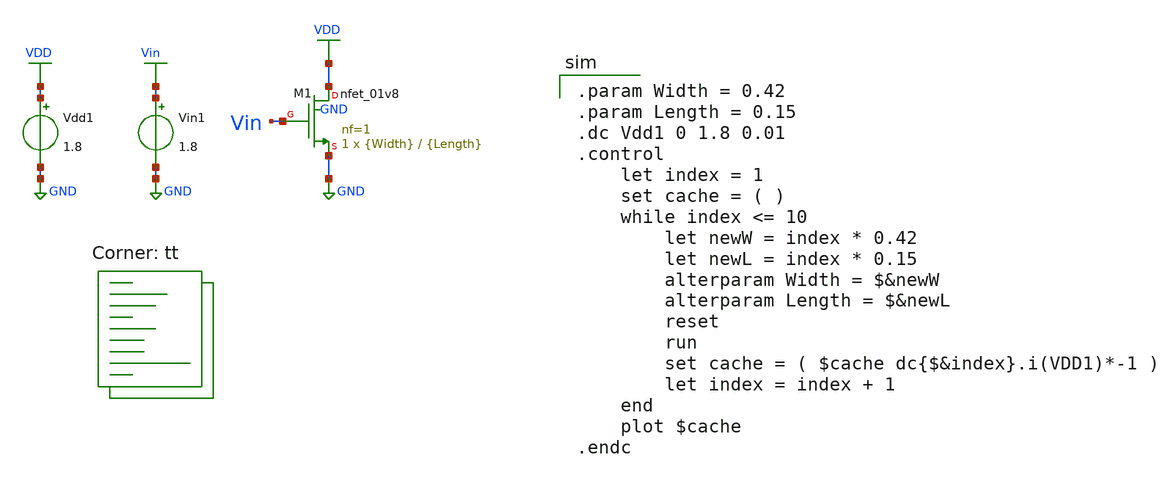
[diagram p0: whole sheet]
** sch_path: tutorial-1/source/q1c.sch
**.subckt q1c
Vdd1 VDD GND 1.8
Vin1 Vin GND 1.8
XM1 VDD Vin GND GND sky130_fd_pr__nfet_01v8 L={Length} W={Width} nf=1 ad='int((nf+1)/2) * W/nf * 0.29'
+ as='int((nf+2)/2) * W/nf * 0.29' pd='2*int((nf+1)/2) * (W/nf + 0.29)' ps='2*int((nf+2)/2) * (W/nf + 0.29)'
+ nrd='0.29 / W' nrs='0.29 / W' sa=0 sb=0 sd=0 mult=1 m=1
**** begin user architecture code
.lib $::SKYWATER_MODELS/sky130.lib.spice tt

.param Width = 0.42
.param Length = 0.15
.dc Vdd1 0 1.8 0.01
.control
    let index = 1
    set cache = ( )
    while index <= 10
        let newW = index * 0.42
        let newL = index * 0.15
        alterparam Width = $&newW
        alterparam Length = $&newL
        reset
        run
        set cache = ( $cache dc{$&index}.i(VDD1)*-1 )
        let index = index + 1
    end
    plot $cache
.endc

**** end user architecture code
**.ends
.GLOBAL VDD
.GLOBAL GND
.GLOBAL Vin
.end
